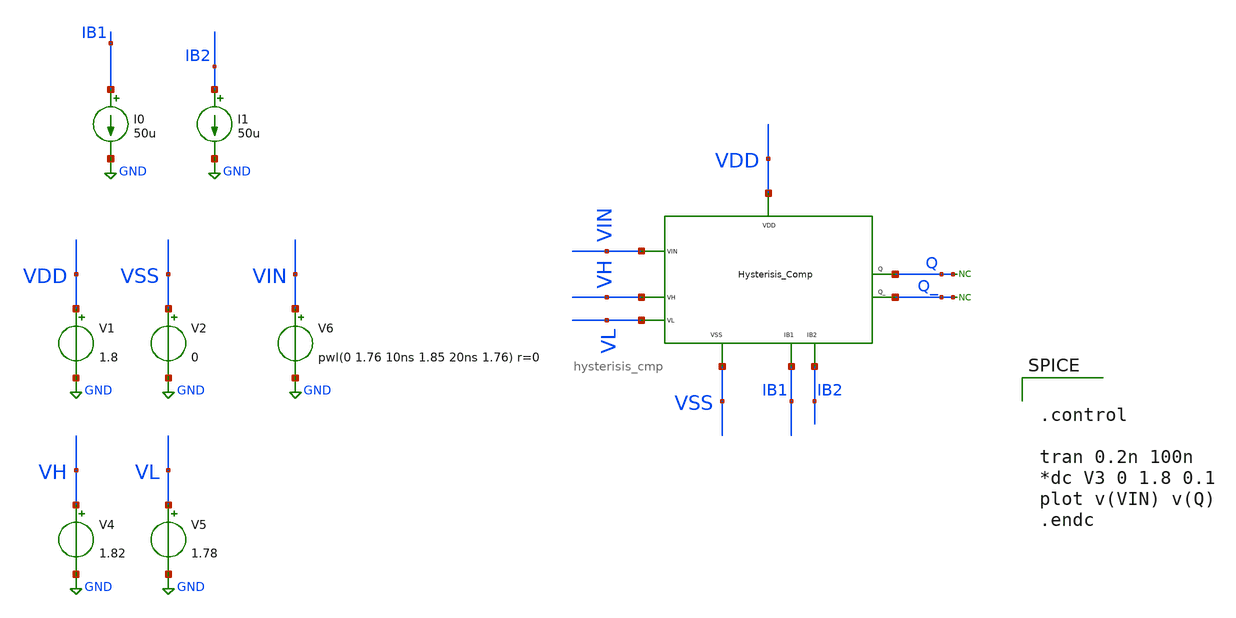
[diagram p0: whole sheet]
** sch_path: xschem/DC_DC_Converter_xschem/OTHERS/DC_DC_Converter_5/Hysterisis_Comparator/hysterisis_cmp_tb.sch
**.subckt hysterisis_cmp_tb
* noconn Q
* noconn Q_
V1 VDD GND 1.8
V2 VSS GND 0
V4 VH GND 1.82
V5 VL GND 1.78
I0 IB1 GND 50u
I1 IB2 GND 50u
V6 VIN GND pwl(0 1.76 10ns 1.85 20ns 1.76) r=0
XM1 VDD VSS VIN VH VL IB1 IB2 Q Q_ hysterisis_cmp
**** begin user architecture code

** opencircuitdesign pdks install
.lib $::SKYWATER_MODELS/sky130.lib.spice tt




.control

tran 0.2n 100n
*dc V3 0 1.8 0.1
plot v(VIN) v(Q)
.endc


**** end user architecture code
**.ends
.GLOBAL GND
.end
